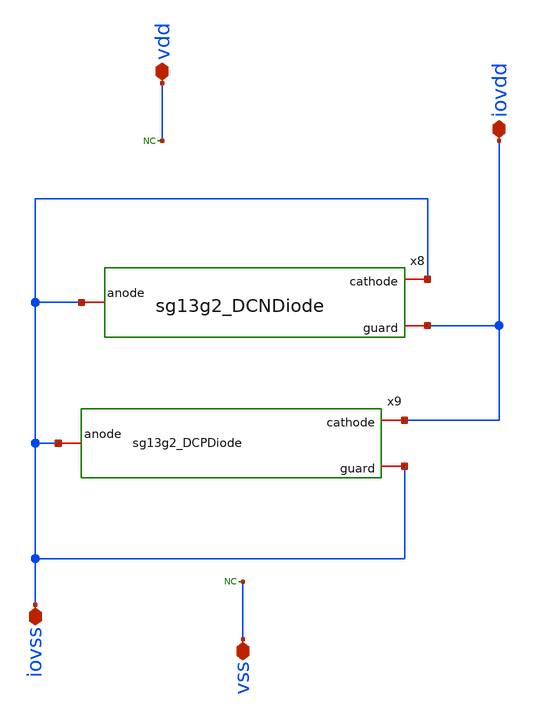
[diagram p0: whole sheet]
** sch_path: CDR4176-main/schematic/xschem/project_io/sg13g2_IOPadIOVss/sg13g2_IOPadIOVss.sch
**.subckt sg13g2_IOPadIOVss iovss iovdd vdd vss
*.iopin iovss
*.iopin iovdd
*.iopin vdd
*.iopin vss
x8 iovss iovss iovdd sg13g2_DCNDiode
x9 iovdd iovss iovss sg13g2_DCPDiode
* noconn vdd
* noconn vss
**.ends

* expanding   symbol:  project_io/sg13g2_DCNDiode/sg13g2_DCNDiode.sym # of pins=3
** sym_path: project_io/sg13g2_DCNDiode/sg13g2_DCNDiode.sym
** sch_path: project_io/sg13g2_DCNDiode/sg13g2_DCNDiode.sch
.subckt sg13g2_DCNDiode cathode anode guard
*.iopin cathode
*.iopin anode
*.iopin guard
XD1 anode cathode dantenna l=1.26u w=27.78u
XD2 anode cathode dantenna l=1.26u w=27.78u
.ends


* expanding   symbol:  project_io/sg13g2_DCPDiode/sg13g2_DCPDiode.sym # of pins=3
** sym_path: project_io/sg13g2_DCPDiode/sg13g2_DCPDiode.sym
** sch_path: project_io/sg13g2_DCPDiode/sg13g2_DCPDiode.sch
.subckt sg13g2_DCPDiode cathode anode guard
*.iopin cathode
*.iopin anode
*.iopin guard
XD1 anode cathode dpantenna l=1.26u w=27.78u
XD2 anode cathode dpantenna l=1.26u w=27.78u
.ends

.end
